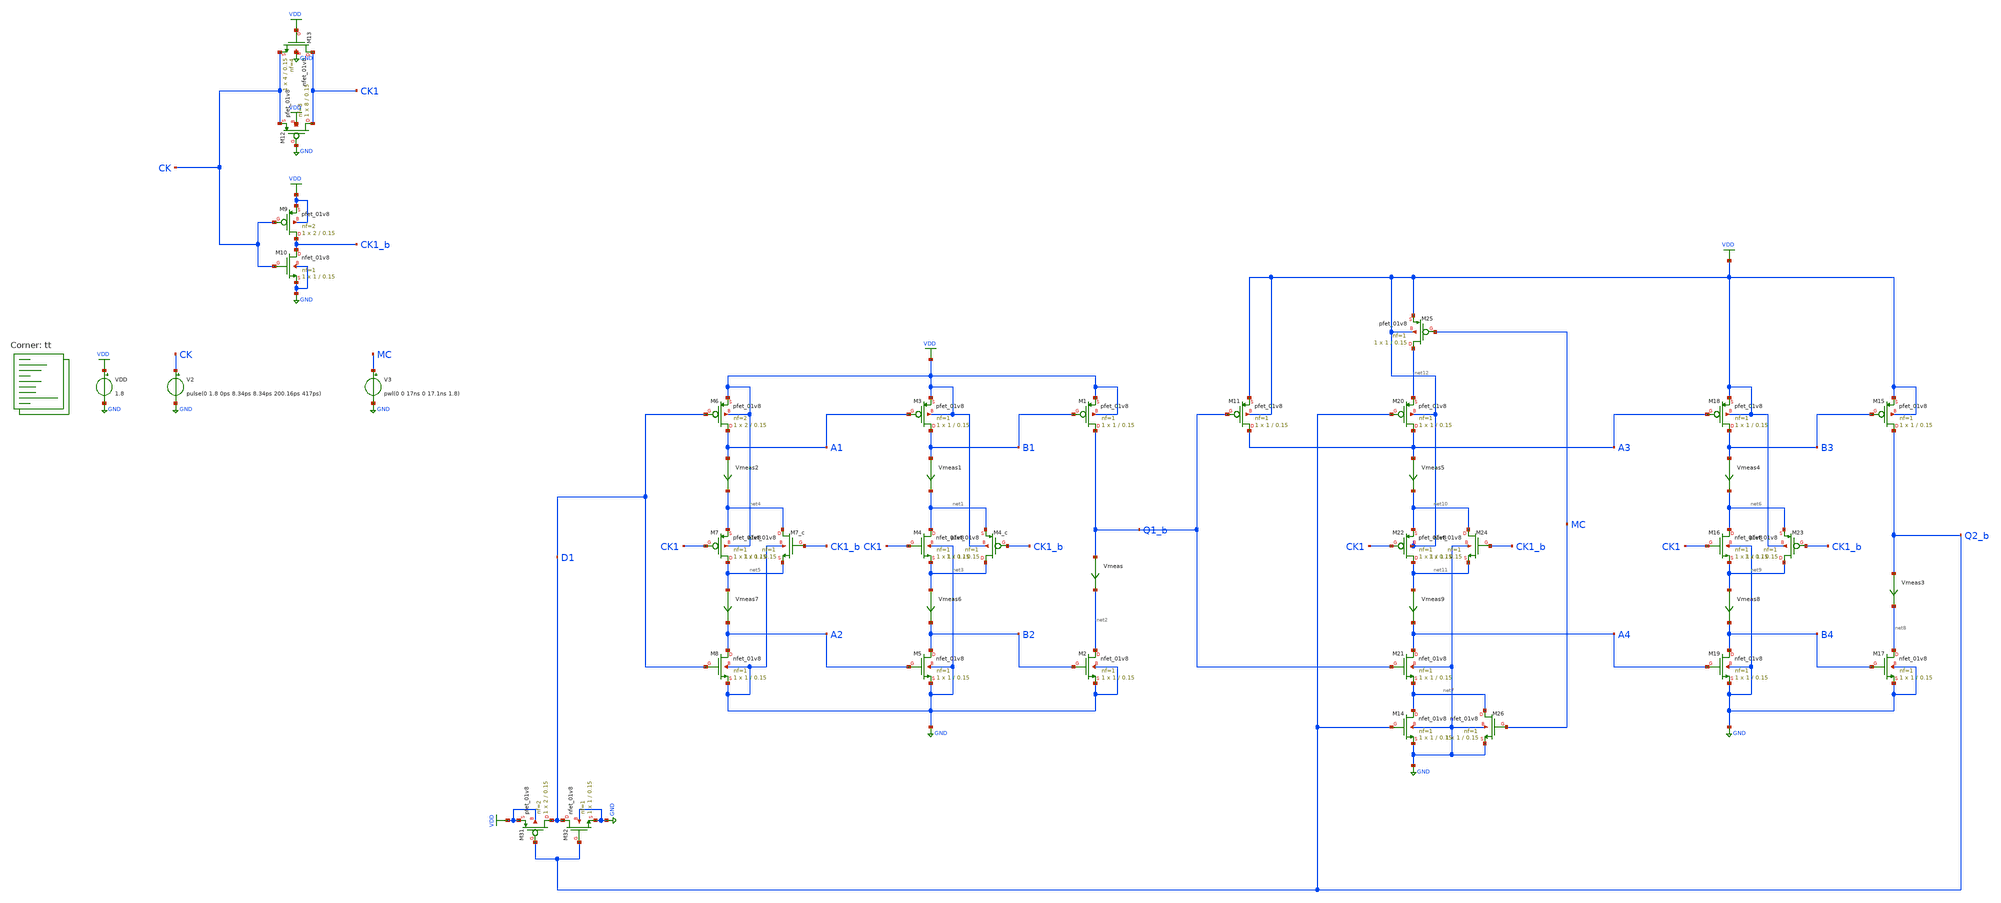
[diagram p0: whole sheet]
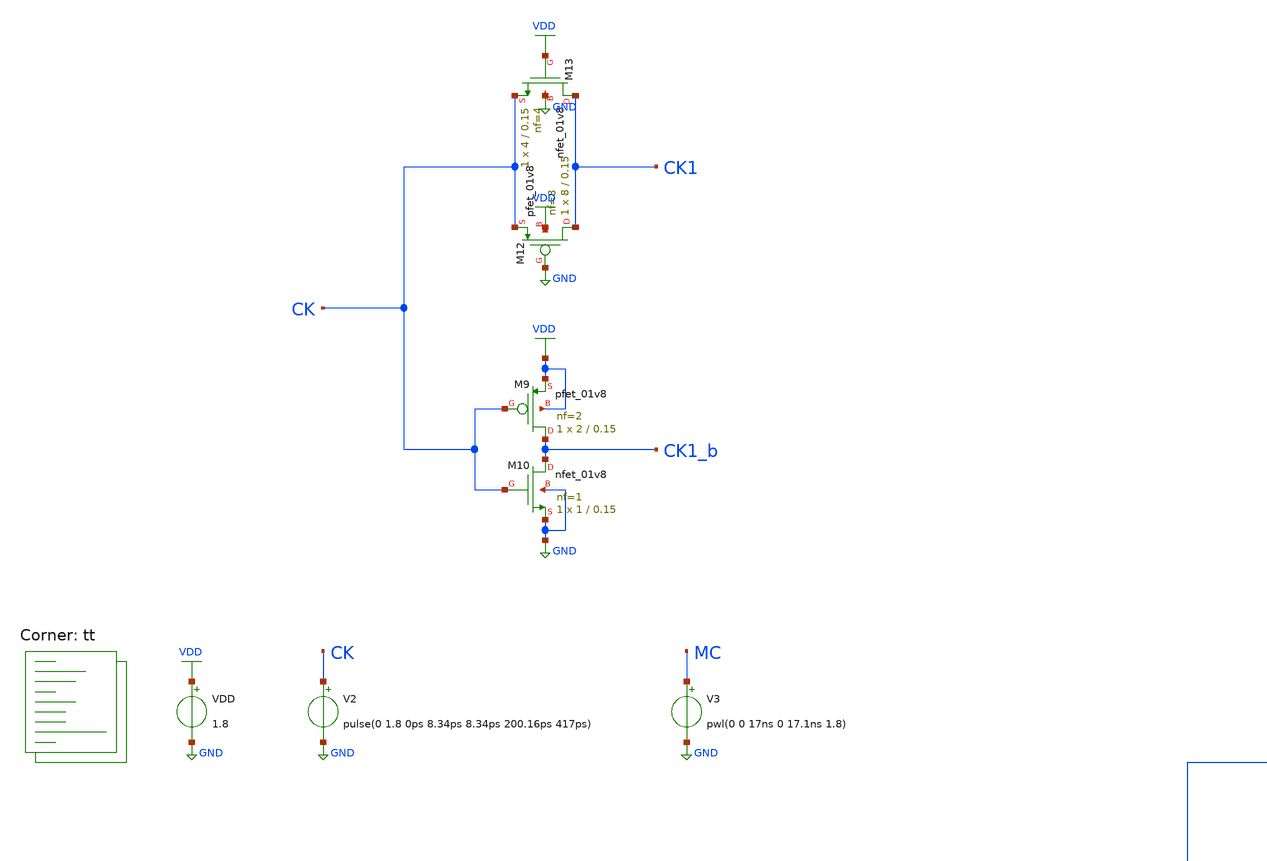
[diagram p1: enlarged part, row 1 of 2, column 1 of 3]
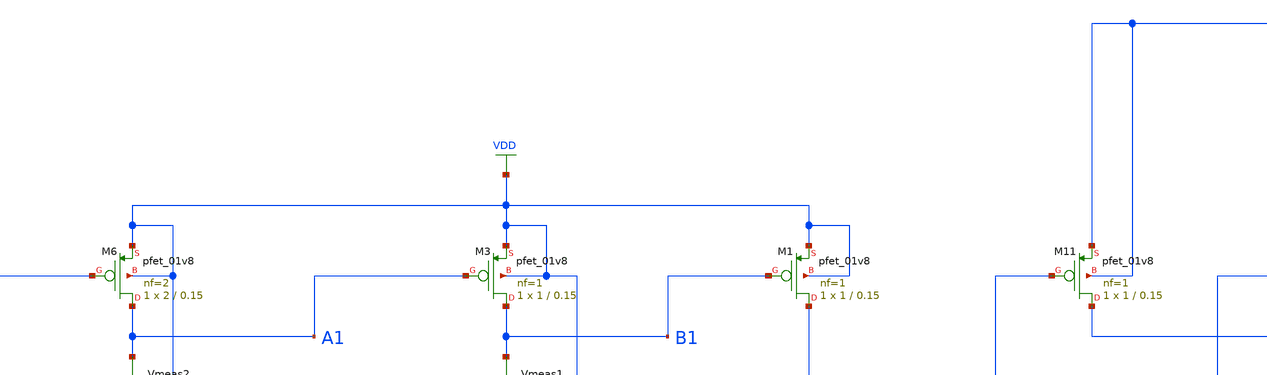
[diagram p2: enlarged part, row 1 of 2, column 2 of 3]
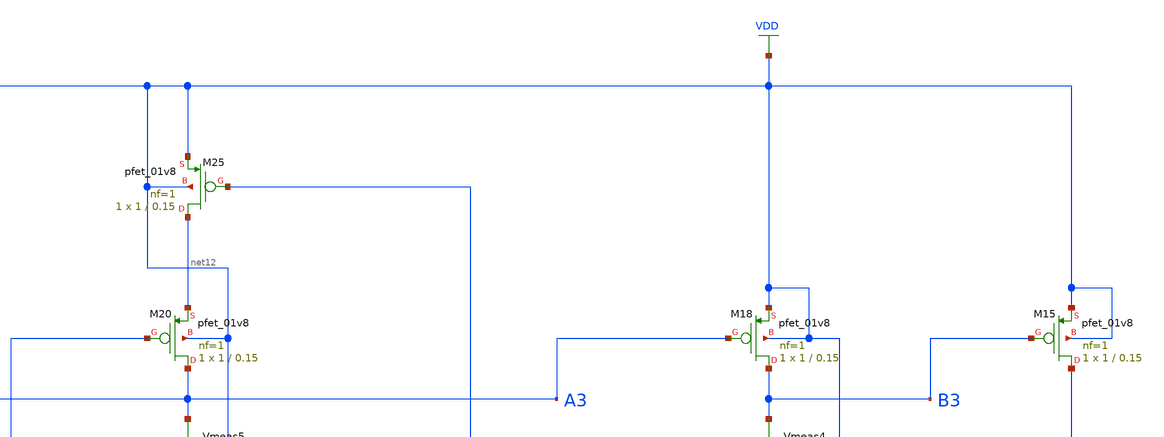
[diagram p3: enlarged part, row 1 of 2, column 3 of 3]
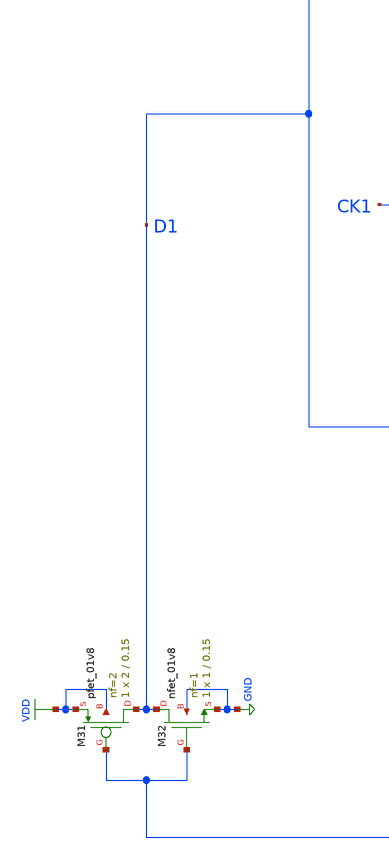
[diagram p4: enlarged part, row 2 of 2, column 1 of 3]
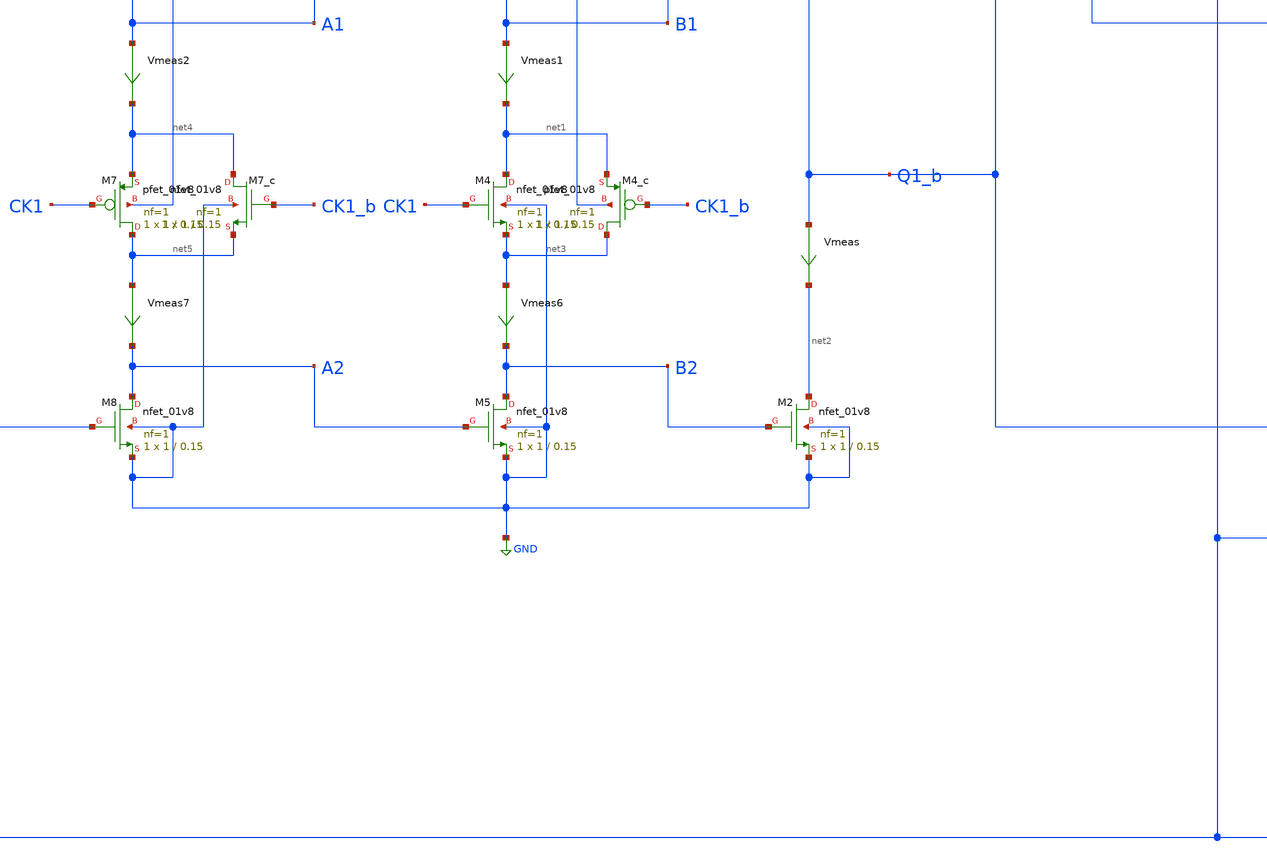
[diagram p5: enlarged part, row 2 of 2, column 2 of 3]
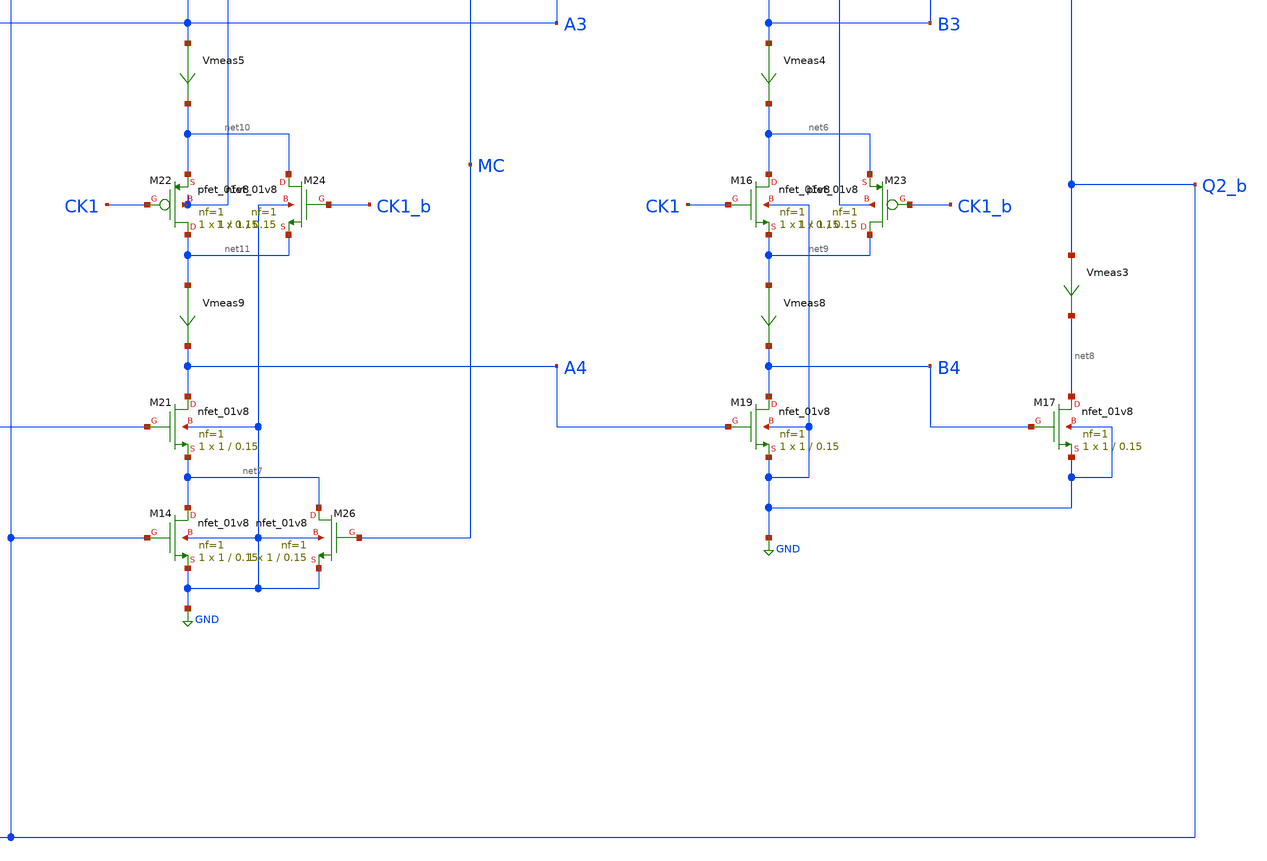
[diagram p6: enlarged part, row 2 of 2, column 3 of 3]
** sch_path: projects/pll/divider/xschem_ngspice/tb_TSPC_FF_comp_sw_divide3_4.sch
**.subckt tb_TSPC_FF_comp_sw_divide3_4
VDD VDD GND 1.8
XM1 Q1_b B1 VDD VDD sky130_fd_pr__pfet_01v8 L=0.15 W=1 nf=1 ad='int((nf+1)/2) * W/nf * 0.29' as='int((nf+2)/2) * W/nf * 0.29'
+ pd='2*int((nf+1)/2) * (W/nf + 0.29)' ps='2*int((nf+2)/2) * (W/nf + 0.29)' nrd='0.29 / W' nrs='0.29 / W'
+ sa=0 sb=0 sd=0 mult=1 m=1
XM4 net1 CK1 net3 GND sky130_fd_pr__nfet_01v8 L=0.15 W=1 nf=1 ad='int((nf+1)/2) * W/nf * 0.29' as='int((nf+2)/2) * W/nf * 0.29'
+ pd='2*int((nf+1)/2) * (W/nf + 0.29)' ps='2*int((nf+2)/2) * (W/nf + 0.29)' nrd='0.29 / W' nrs='0.29 / W'
+ sa=0 sb=0 sd=0 mult=1 m=1
Vmeas Q1_b net2 0
.save i(vmeas)
XM2 net2 B2 GND GND sky130_fd_pr__nfet_01v8 L=0.15 W=1 nf=1 ad='int((nf+1)/2) * W/nf * 0.29' as='int((nf+2)/2) * W/nf * 0.29'
+ pd='2*int((nf+1)/2) * (W/nf + 0.29)' ps='2*int((nf+2)/2) * (W/nf + 0.29)' nrd='0.29 / W' nrs='0.29 / W'
+ sa=0 sb=0 sd=0 mult=1 m=1
XM3 B1 A1 VDD VDD sky130_fd_pr__pfet_01v8 L=0.15 W=1 nf=1 ad='int((nf+1)/2) * W/nf * 0.29' as='int((nf+2)/2) * W/nf * 0.29'
+ pd='2*int((nf+1)/2) * (W/nf + 0.29)' ps='2*int((nf+2)/2) * (W/nf + 0.29)' nrd='0.29 / W' nrs='0.29 / W'
+ sa=0 sb=0 sd=0 mult=1 m=1
XM5 B2 A2 GND GND sky130_fd_pr__nfet_01v8 L=0.15 W=1 nf=1 ad='int((nf+1)/2) * W/nf * 0.29' as='int((nf+2)/2) * W/nf * 0.29'
+ pd='2*int((nf+1)/2) * (W/nf + 0.29)' ps='2*int((nf+2)/2) * (W/nf + 0.29)' nrd='0.29 / W' nrs='0.29 / W'
+ sa=0 sb=0 sd=0 mult=1 m=1
Vmeas1 B1 net1 0
.save i(vmeas1)
XM6 A1 D1 VDD VDD sky130_fd_pr__pfet_01v8 L=0.15 W=2 nf=2 ad='int((nf+1)/2) * W/nf * 0.29' as='int((nf+2)/2) * W/nf * 0.29'
+ pd='2*int((nf+1)/2) * (W/nf + 0.29)' ps='2*int((nf+2)/2) * (W/nf + 0.29)' nrd='0.29 / W' nrs='0.29 / W'
+ sa=0 sb=0 sd=0 mult=1 m=1
XM8 A2 D1 GND GND sky130_fd_pr__nfet_01v8 L=0.15 W=1 nf=1 ad='int((nf+1)/2) * W/nf * 0.29' as='int((nf+2)/2) * W/nf * 0.29'
+ pd='2*int((nf+1)/2) * (W/nf + 0.29)' ps='2*int((nf+2)/2) * (W/nf + 0.29)' nrd='0.29 / W' nrs='0.29 / W'
+ sa=0 sb=0 sd=0 mult=1 m=1
Vmeas2 A1 net4 0
.save i(vmeas2)
XM7 net5 CK1 net4 VDD sky130_fd_pr__pfet_01v8 L=0.15 W=1 nf=1 ad='int((nf+1)/2) * W/nf * 0.29' as='int((nf+2)/2) * W/nf * 0.29'
+ pd='2*int((nf+1)/2) * (W/nf + 0.29)' ps='2*int((nf+2)/2) * (W/nf + 0.29)' nrd='0.29 / W' nrs='0.29 / W'
+ sa=0 sb=0 sd=0 mult=1 m=1
XM4_c net3 CK1_b net1 VDD sky130_fd_pr__pfet_01v8 L=0.15 W=1 nf=1 ad='int((nf+1)/2) * W/nf * 0.29' as='int((nf+2)/2) * W/nf * 0.29'
+ pd='2*int((nf+1)/2) * (W/nf + 0.29)' ps='2*int((nf+2)/2) * (W/nf + 0.29)' nrd='0.29 / W' nrs='0.29 / W'
+ sa=0 sb=0 sd=0 mult=1 m=1
XM7_c net4 CK1_b net5 GND sky130_fd_pr__nfet_01v8 L=0.15 W=1 nf=1 ad='int((nf+1)/2) * W/nf * 0.29' as='int((nf+2)/2) * W/nf * 0.29'
+ pd='2*int((nf+1)/2) * (W/nf + 0.29)' ps='2*int((nf+2)/2) * (W/nf + 0.29)' nrd='0.29 / W' nrs='0.29 / W'
+ sa=0 sb=0 sd=0 mult=1 m=1
XM12 CK1 GND CK VDD sky130_fd_pr__pfet_01v8 L=0.15 W=8 nf=8 ad='int((nf+1)/2) * W/nf * 0.29' as='int((nf+2)/2) * W/nf * 0.29'
+ pd='2*int((nf+1)/2) * (W/nf + 0.29)' ps='2*int((nf+2)/2) * (W/nf + 0.29)' nrd='0.29 / W' nrs='0.29 / W'
+ sa=0 sb=0 sd=0 mult=1 m=1
XM13 CK1 VDD CK GND sky130_fd_pr__nfet_01v8 L=0.15 W=4 nf=4 ad='int((nf+1)/2) * W/nf * 0.29' as='int((nf+2)/2) * W/nf * 0.29'
+ pd='2*int((nf+1)/2) * (W/nf + 0.29)' ps='2*int((nf+2)/2) * (W/nf + 0.29)' nrd='0.29 / W' nrs='0.29 / W'
+ sa=0 sb=0 sd=0 mult=1 m=1
XM9 CK1_b CK VDD VDD sky130_fd_pr__pfet_01v8 L=0.15 W=2 nf=2 ad='int((nf+1)/2) * W/nf * 0.29' as='int((nf+2)/2) * W/nf * 0.29'
+ pd='2*int((nf+1)/2) * (W/nf + 0.29)' ps='2*int((nf+2)/2) * (W/nf + 0.29)' nrd='0.29 / W' nrs='0.29 / W'
+ sa=0 sb=0 sd=0 mult=1 m=1
XM10 CK1_b CK GND GND sky130_fd_pr__nfet_01v8 L=0.15 W=1 nf=1 ad='int((nf+1)/2) * W/nf * 0.29' as='int((nf+2)/2) * W/nf * 0.29'
+ pd='2*int((nf+1)/2) * (W/nf + 0.29)' ps='2*int((nf+2)/2) * (W/nf + 0.29)' nrd='0.29 / W' nrs='0.29 / W'
+ sa=0 sb=0 sd=0 mult=1 m=1
XM15 Q2_b B3 VDD VDD sky130_fd_pr__pfet_01v8 L=0.15 W=1 nf=1 ad='int((nf+1)/2) * W/nf * 0.29' as='int((nf+2)/2) * W/nf * 0.29'
+ pd='2*int((nf+1)/2) * (W/nf + 0.29)' ps='2*int((nf+2)/2) * (W/nf + 0.29)' nrd='0.29 / W' nrs='0.29 / W'
+ sa=0 sb=0 sd=0 mult=1 m=1
XM16 net6 CK1 net9 GND sky130_fd_pr__nfet_01v8 L=0.15 W=1 nf=1 ad='int((nf+1)/2) * W/nf * 0.29' as='int((nf+2)/2) * W/nf * 0.29'
+ pd='2*int((nf+1)/2) * (W/nf + 0.29)' ps='2*int((nf+2)/2) * (W/nf + 0.29)' nrd='0.29 / W' nrs='0.29 / W'
+ sa=0 sb=0 sd=0 mult=1 m=1
Vmeas3 Q2_b net8 0
.save i(vmeas3)
XM17 net8 B4 GND GND sky130_fd_pr__nfet_01v8 L=0.15 W=1 nf=1 ad='int((nf+1)/2) * W/nf * 0.29' as='int((nf+2)/2) * W/nf * 0.29'
+ pd='2*int((nf+1)/2) * (W/nf + 0.29)' ps='2*int((nf+2)/2) * (W/nf + 0.29)' nrd='0.29 / W' nrs='0.29 / W'
+ sa=0 sb=0 sd=0 mult=1 m=1
XM18 B3 A3 VDD VDD sky130_fd_pr__pfet_01v8 L=0.15 W=1 nf=1 ad='int((nf+1)/2) * W/nf * 0.29' as='int((nf+2)/2) * W/nf * 0.29'
+ pd='2*int((nf+1)/2) * (W/nf + 0.29)' ps='2*int((nf+2)/2) * (W/nf + 0.29)' nrd='0.29 / W' nrs='0.29 / W'
+ sa=0 sb=0 sd=0 mult=1 m=1
XM19 B4 A4 GND GND sky130_fd_pr__nfet_01v8 L=0.15 W=1 nf=1 ad='int((nf+1)/2) * W/nf * 0.29' as='int((nf+2)/2) * W/nf * 0.29'
+ pd='2*int((nf+1)/2) * (W/nf + 0.29)' ps='2*int((nf+2)/2) * (W/nf + 0.29)' nrd='0.29 / W' nrs='0.29 / W'
+ sa=0 sb=0 sd=0 mult=1 m=1
Vmeas4 B3 net6 0
.save i(vmeas4)
XM20 A3 Q2_b net12 VDD sky130_fd_pr__pfet_01v8 L=0.15 W=1 nf=1 ad='int((nf+1)/2) * W/nf * 0.29' as='int((nf+2)/2) * W/nf * 0.29'
+ pd='2*int((nf+1)/2) * (W/nf + 0.29)' ps='2*int((nf+2)/2) * (W/nf + 0.29)' nrd='0.29 / W' nrs='0.29 / W'
+ sa=0 sb=0 sd=0 mult=1 m=1
XM21 A4 Q1_b net7 GND sky130_fd_pr__nfet_01v8 L=0.15 W=1 nf=1 ad='int((nf+1)/2) * W/nf * 0.29' as='int((nf+2)/2) * W/nf * 0.29'
+ pd='2*int((nf+1)/2) * (W/nf + 0.29)' ps='2*int((nf+2)/2) * (W/nf + 0.29)' nrd='0.29 / W' nrs='0.29 / W'
+ sa=0 sb=0 sd=0 mult=1 m=1
Vmeas5 A3 net10 0
.save i(vmeas5)
XM22 net11 CK1 net10 VDD sky130_fd_pr__pfet_01v8 L=0.15 W=1 nf=1 ad='int((nf+1)/2) * W/nf * 0.29' as='int((nf+2)/2) * W/nf * 0.29'
+ pd='2*int((nf+1)/2) * (W/nf + 0.29)' ps='2*int((nf+2)/2) * (W/nf + 0.29)' nrd='0.29 / W' nrs='0.29 / W'
+ sa=0 sb=0 sd=0 mult=1 m=1
XM23 net9 CK1_b net6 VDD sky130_fd_pr__pfet_01v8 L=0.15 W=1 nf=1 ad='int((nf+1)/2) * W/nf * 0.29' as='int((nf+2)/2) * W/nf * 0.29'
+ pd='2*int((nf+1)/2) * (W/nf + 0.29)' ps='2*int((nf+2)/2) * (W/nf + 0.29)' nrd='0.29 / W' nrs='0.29 / W'
+ sa=0 sb=0 sd=0 mult=1 m=1
XM24 net10 CK1_b net11 GND sky130_fd_pr__nfet_01v8 L=0.15 W=1 nf=1 ad='int((nf+1)/2) * W/nf * 0.29' as='int((nf+2)/2) * W/nf * 0.29'
+ pd='2*int((nf+1)/2) * (W/nf + 0.29)' ps='2*int((nf+2)/2) * (W/nf + 0.29)' nrd='0.29 / W' nrs='0.29 / W'
+ sa=0 sb=0 sd=0 mult=1 m=1
Vmeas6 net3 B2 0
.save i(vmeas6)
Vmeas7 net5 A2 0
.save i(vmeas7)
Vmeas8 net9 B4 0
.save i(vmeas8)
Vmeas9 net11 A4 0
.save i(vmeas9)
V2 CK GND pulse(0 1.8 0ps 8.34ps 8.34ps 200.16ps 417ps)
XM31 D1 Q2_b VDD VDD sky130_fd_pr__pfet_01v8 L=0.15 W=2 nf=2 ad='int((nf+1)/2) * W/nf * 0.29' as='int((nf+2)/2) * W/nf * 0.29'
+ pd='2*int((nf+1)/2) * (W/nf + 0.29)' ps='2*int((nf+2)/2) * (W/nf + 0.29)' nrd='0.29 / W' nrs='0.29 / W'
+ sa=0 sb=0 sd=0 mult=1 m=1
XM32 D1 Q2_b GND GND sky130_fd_pr__nfet_01v8 L=0.15 W=1 nf=1 ad='int((nf+1)/2) * W/nf * 0.29' as='int((nf+2)/2) * W/nf * 0.29'
+ pd='2*int((nf+1)/2) * (W/nf + 0.29)' ps='2*int((nf+2)/2) * (W/nf + 0.29)' nrd='0.29 / W' nrs='0.29 / W'
+ sa=0 sb=0 sd=0 mult=1 m=1
XM11 A3 Q1_b VDD VDD sky130_fd_pr__pfet_01v8 L=0.15 W=1 nf=1 ad='int((nf+1)/2) * W/nf * 0.29' as='int((nf+2)/2) * W/nf * 0.29'
+ pd='2*int((nf+1)/2) * (W/nf + 0.29)' ps='2*int((nf+2)/2) * (W/nf + 0.29)' nrd='0.29 / W' nrs='0.29 / W'
+ sa=0 sb=0 sd=0 mult=1 m=1
XM14 net7 Q2_b GND GND sky130_fd_pr__nfet_01v8 L=0.15 W=1 nf=1 ad='int((nf+1)/2) * W/nf * 0.29' as='int((nf+2)/2) * W/nf * 0.29'
+ pd='2*int((nf+1)/2) * (W/nf + 0.29)' ps='2*int((nf+2)/2) * (W/nf + 0.29)' nrd='0.29 / W' nrs='0.29 / W'
+ sa=0 sb=0 sd=0 mult=1 m=1
XM25 net12 MC VDD VDD sky130_fd_pr__pfet_01v8 L=0.15 W=1 nf=1 ad='int((nf+1)/2) * W/nf * 0.29' as='int((nf+2)/2) * W/nf * 0.29'
+ pd='2*int((nf+1)/2) * (W/nf + 0.29)' ps='2*int((nf+2)/2) * (W/nf + 0.29)' nrd='0.29 / W' nrs='0.29 / W'
+ sa=0 sb=0 sd=0 mult=1 m=1
XM26 net7 MC GND GND sky130_fd_pr__nfet_01v8 L=0.15 W=1 nf=1 ad='int((nf+1)/2) * W/nf * 0.29' as='int((nf+2)/2) * W/nf * 0.29'
+ pd='2*int((nf+1)/2) * (W/nf + 0.29)' ps='2*int((nf+2)/2) * (W/nf + 0.29)' nrd='0.29 / W' nrs='0.29 / W'
+ sa=0 sb=0 sd=0 mult=1 m=1
V3 MC GND pwl(0 0 17ns 0 17.1ns 1.8)
**** begin user architecture code



.include /foss/pdks/sky130A/libs.ref/sky130_fd_sc_hd/spice/sky130_fd_sc_hd.spice

.option method=gear
.option wnflag=1
.option savecurrents

.save @m.xm1.msky130_fd_pr__pfet_01v8[gm] @m.xm2.msky130_fd_pr__nfet_01v8[gm] @m.xm3.msky130_fd_pr__pfet_01v8[gm] @m.xm4.msky130_fd_pr__nfet_01v8[gm] @m.xm4_c.msky130_fd_pr__pfet_01v8[gm] @m.xm5.msky130_fd_pr__nfet_01v8[gm] @m.xm6.msky130_fd_pr__pfet_01v8[gm] @m.xm7.msky130_fd_pr__pfet_01v8[gm] @m.xm7_c.msky130_fd_pr__nfet_01v8[gm] @m.xm8.msky130_fd_pr__nfet_01v8[gm]

*.ic v(d)=0
*.ic v(q)=0
*.ic v(q1)=0

.control

  save v(d1) v(d2) v(q1) v(q2) v(q1_b) v(q2_b) v(q3) v(a1) v(a2) v(a3) v(a4) v(b1) v(b2) v(b3) v(b4)
+ v(ck) v(ck1) v(ck1_b) v(mc)
  * save all
  * tran 0.1n 1u
  tran 1p 40n

  remzerovec
  write tb_TSPC_FF_comp_sw_divide3_4.raw
  * set appendwrite

.endc



.lib $::SKYWATER_MODELS/sky130.lib.spice tt
**** end user architecture code
**.ends
.GLOBAL GND
.GLOBAL VDD
.end
